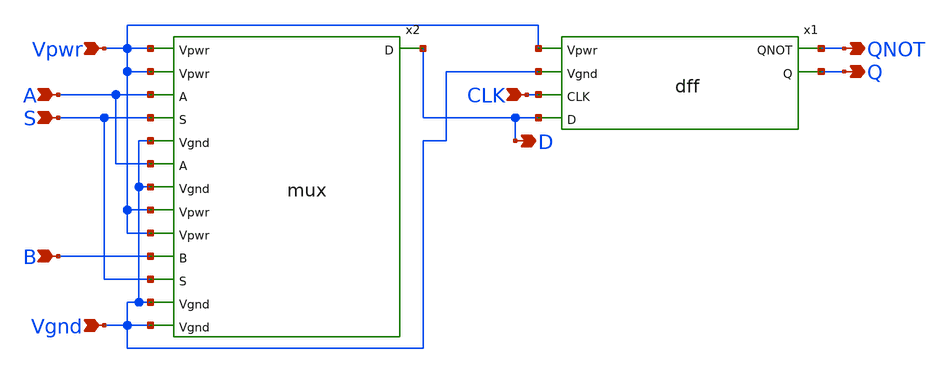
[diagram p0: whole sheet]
** sch_path: MUXDFF/muxdd.sch
**.subckt muxdd CLK QNOT Vpwr Vgnd A S B Q D
*.ipin CLK
*.opin QNOT
*.ipin Vpwr
*.ipin Vgnd
*.ipin A
*.ipin S
*.ipin B
*.opin Q
*.opin D
x1 QNOT Vpwr Vgnd CLK Q D dff
x2 Vpwr A S Vgnd D B mux
**.ends
.end
